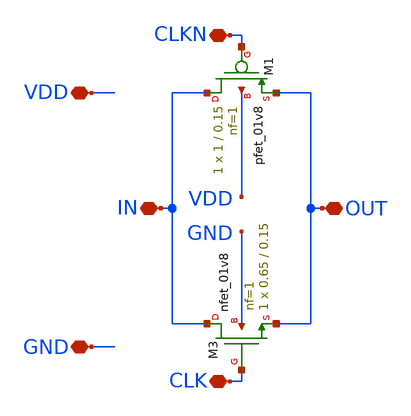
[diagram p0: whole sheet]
** sch_path: DIV/passgate_DIV/passgate_DIV.sch
**.subckt passgate_DIV VDD OUT GND IN CLKN CLK
*.iopin VDD
*.iopin OUT
*.iopin GND
*.iopin IN
*.iopin CLKN
*.iopin CLK
XM3 IN CLK OUT GND sky130_fd_pr__nfet_01v8 L=0.15 W=0.65 nf=1 ad='int((nf+1)/2) * W/nf * 0.29' as='int((nf+2)/2) * W/nf * 0.29'
+ pd='2*int((nf+1)/2) * (W/nf + 0.29)' ps='2*int((nf+2)/2) * (W/nf + 0.29)' nrd='0.29 / W' nrs='0.29 / W'
+ sa=0 sb=0 sd=0 mult=1 m=1
XM1 IN CLKN OUT VDD sky130_fd_pr__pfet_01v8 L=0.15 W=1 nf=1 ad='int((nf+1)/2) * W/nf * 0.29' as='int((nf+2)/2) * W/nf * 0.29'
+ pd='2*int((nf+1)/2) * (W/nf + 0.29)' ps='2*int((nf+2)/2) * (W/nf + 0.29)' nrd='0.29 / W' nrs='0.29 / W'
+ sa=0 sb=0 sd=0 mult=1 m=1
**.ends
.end
